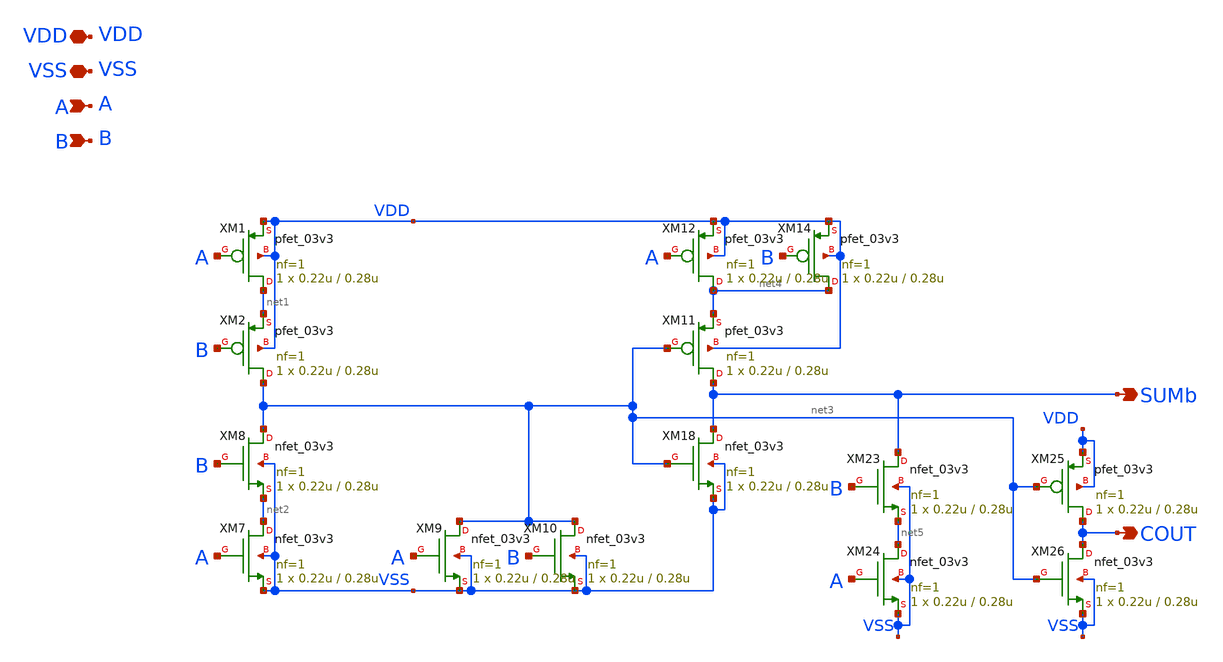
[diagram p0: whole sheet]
** sch_path: CAD4/full_adder_cin_1.sch
**.subckt full_adder_cin_1 VDD VSS A B SUMb COUT
*.iopin VDD
*.iopin VSS
*.ipin A
*.ipin B
*.opin SUMb
*.opin COUT
XM1 net1 A VDD VDD pfet_03v3 L=0.28u W=0.22u nf=1 ad='int((nf+1)/2) * W/nf * 0.18u' as='int((nf+2)/2) * W/nf * 0.18u'
+ pd='2*int((nf+1)/2) * (W/nf + 0.18u)' ps='2*int((nf+2)/2) * (W/nf + 0.18u)' nrd='0.18u / W' nrs='0.18u / W'
+ sa=0 sb=0 sd=0 m=1
XM2 net3 B net1 VDD pfet_03v3 L=0.28u W=0.22u nf=1 ad='int((nf+1)/2) * W/nf * 0.18u' as='int((nf+2)/2) * W/nf * 0.18u'
+ pd='2*int((nf+1)/2) * (W/nf + 0.18u)' ps='2*int((nf+2)/2) * (W/nf + 0.18u)' nrd='0.18u / W' nrs='0.18u / W'
+ sa=0 sb=0 sd=0 m=1
XM7 net2 A VSS VSS nfet_03v3 L=0.28u W=0.22u nf=1 ad='int((nf+1)/2) * W/nf * 0.18u' as='int((nf+2)/2) * W/nf * 0.18u'
+ pd='2*int((nf+1)/2) * (W/nf + 0.18u)' ps='2*int((nf+2)/2) * (W/nf + 0.18u)' nrd='0.18u / W' nrs='0.18u / W'
+ sa=0 sb=0 sd=0 m=1
XM8 net3 B net2 VSS nfet_03v3 L=0.28u W=0.22u nf=1 ad='int((nf+1)/2) * W/nf * 0.18u' as='int((nf+2)/2) * W/nf * 0.18u'
+ pd='2*int((nf+1)/2) * (W/nf + 0.18u)' ps='2*int((nf+2)/2) * (W/nf + 0.18u)' nrd='0.18u / W' nrs='0.18u / W'
+ sa=0 sb=0 sd=0 m=1
XM9 net3 A VSS VSS nfet_03v3 L=0.28u W=0.22u nf=1 ad='int((nf+1)/2) * W/nf * 0.18u' as='int((nf+2)/2) * W/nf * 0.18u'
+ pd='2*int((nf+1)/2) * (W/nf + 0.18u)' ps='2*int((nf+2)/2) * (W/nf + 0.18u)' nrd='0.18u / W' nrs='0.18u / W'
+ sa=0 sb=0 sd=0 m=1
XM10 net3 B VSS VSS nfet_03v3 L=0.28u W=0.22u nf=1 ad='int((nf+1)/2) * W/nf * 0.18u' as='int((nf+2)/2) * W/nf * 0.18u'
+ pd='2*int((nf+1)/2) * (W/nf + 0.18u)' ps='2*int((nf+2)/2) * (W/nf + 0.18u)' nrd='0.18u / W' nrs='0.18u / W'
+ sa=0 sb=0 sd=0 m=1
XM11 SUMb net3 net4 VDD pfet_03v3 L=0.28u W=0.22u nf=1 ad='int((nf+1)/2) * W/nf * 0.18u' as='int((nf+2)/2) * W/nf * 0.18u'
+ pd='2*int((nf+1)/2) * (W/nf + 0.18u)' ps='2*int((nf+2)/2) * (W/nf + 0.18u)' nrd='0.18u / W' nrs='0.18u / W'
+ sa=0 sb=0 sd=0 m=1
XM12 net4 A VDD VDD pfet_03v3 L=0.28u W=0.22u nf=1 ad='int((nf+1)/2) * W/nf * 0.18u' as='int((nf+2)/2) * W/nf * 0.18u'
+ pd='2*int((nf+1)/2) * (W/nf + 0.18u)' ps='2*int((nf+2)/2) * (W/nf + 0.18u)' nrd='0.18u / W' nrs='0.18u / W'
+ sa=0 sb=0 sd=0 m=1
XM14 net4 B VDD VDD pfet_03v3 L=0.28u W=0.22u nf=1 ad='int((nf+1)/2) * W/nf * 0.18u' as='int((nf+2)/2) * W/nf * 0.18u'
+ pd='2*int((nf+1)/2) * (W/nf + 0.18u)' ps='2*int((nf+2)/2) * (W/nf + 0.18u)' nrd='0.18u / W' nrs='0.18u / W'
+ sa=0 sb=0 sd=0 m=1
XM18 SUMb net3 VSS VSS nfet_03v3 L=0.28u W=0.22u nf=1 ad='int((nf+1)/2) * W/nf * 0.18u' as='int((nf+2)/2) * W/nf * 0.18u'
+ pd='2*int((nf+1)/2) * (W/nf + 0.18u)' ps='2*int((nf+2)/2) * (W/nf + 0.18u)' nrd='0.18u / W' nrs='0.18u / W'
+ sa=0 sb=0 sd=0 m=1
XM23 SUMb B net5 VSS nfet_03v3 L=0.28u W=0.22u nf=1 ad='int((nf+1)/2) * W/nf * 0.18u' as='int((nf+2)/2) * W/nf * 0.18u'
+ pd='2*int((nf+1)/2) * (W/nf + 0.18u)' ps='2*int((nf+2)/2) * (W/nf + 0.18u)' nrd='0.18u / W' nrs='0.18u / W'
+ sa=0 sb=0 sd=0 m=1
XM24 net5 A VSS VSS nfet_03v3 L=0.28u W=0.22u nf=1 ad='int((nf+1)/2) * W/nf * 0.18u' as='int((nf+2)/2) * W/nf * 0.18u'
+ pd='2*int((nf+1)/2) * (W/nf + 0.18u)' ps='2*int((nf+2)/2) * (W/nf + 0.18u)' nrd='0.18u / W' nrs='0.18u / W'
+ sa=0 sb=0 sd=0 m=1
XM25 COUT net3 VDD VDD pfet_03v3 L=0.28u W=0.22u nf=1 ad='int((nf+1)/2) * W/nf * 0.18u' as='int((nf+2)/2) * W/nf * 0.18u'
+ pd='2*int((nf+1)/2) * (W/nf + 0.18u)' ps='2*int((nf+2)/2) * (W/nf + 0.18u)' nrd='0.18u / W' nrs='0.18u / W'
+ sa=0 sb=0 sd=0 m=1
XM26 COUT net3 VSS VSS nfet_03v3 L=0.28u W=0.22u nf=1 ad='int((nf+1)/2) * W/nf * 0.18u' as='int((nf+2)/2) * W/nf * 0.18u'
+ pd='2*int((nf+1)/2) * (W/nf + 0.18u)' ps='2*int((nf+2)/2) * (W/nf + 0.18u)' nrd='0.18u / W' nrs='0.18u / W'
+ sa=0 sb=0 sd=0 m=1
**.ends
.end
